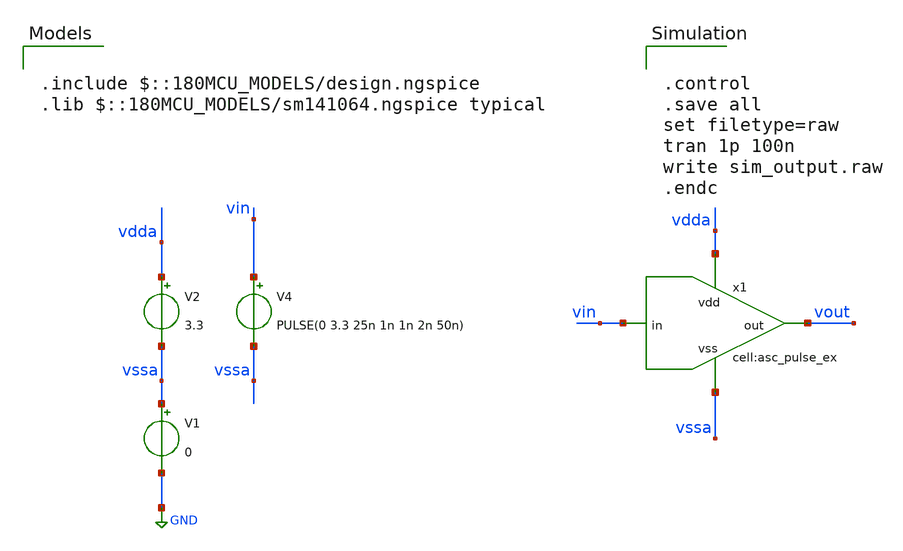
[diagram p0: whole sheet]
** sch_path: designs/libs/tb_analog/tb_asc_pulse_ex/tb_asc_pulse_ex.sch
**.subckt tb_asc_pulse_ex
V1 vssa GND 0
V2 vdda vssa 3.3
V4 vin vssa PULSE(0 3.3 25n 1n 1n 2n 50n)
x1 vin vssa vout vdda asc_pulse_ex
**** begin user architecture code

.include $::180MCU_MODELS/design.ngspice
.lib $::180MCU_MODELS/sm141064.ngspice typical



.control
.save all
set filetype=raw
tran 1p 100n
write sim_output.raw
.endc


**** end user architecture code
**.ends
.GLOBAL GND
.end
